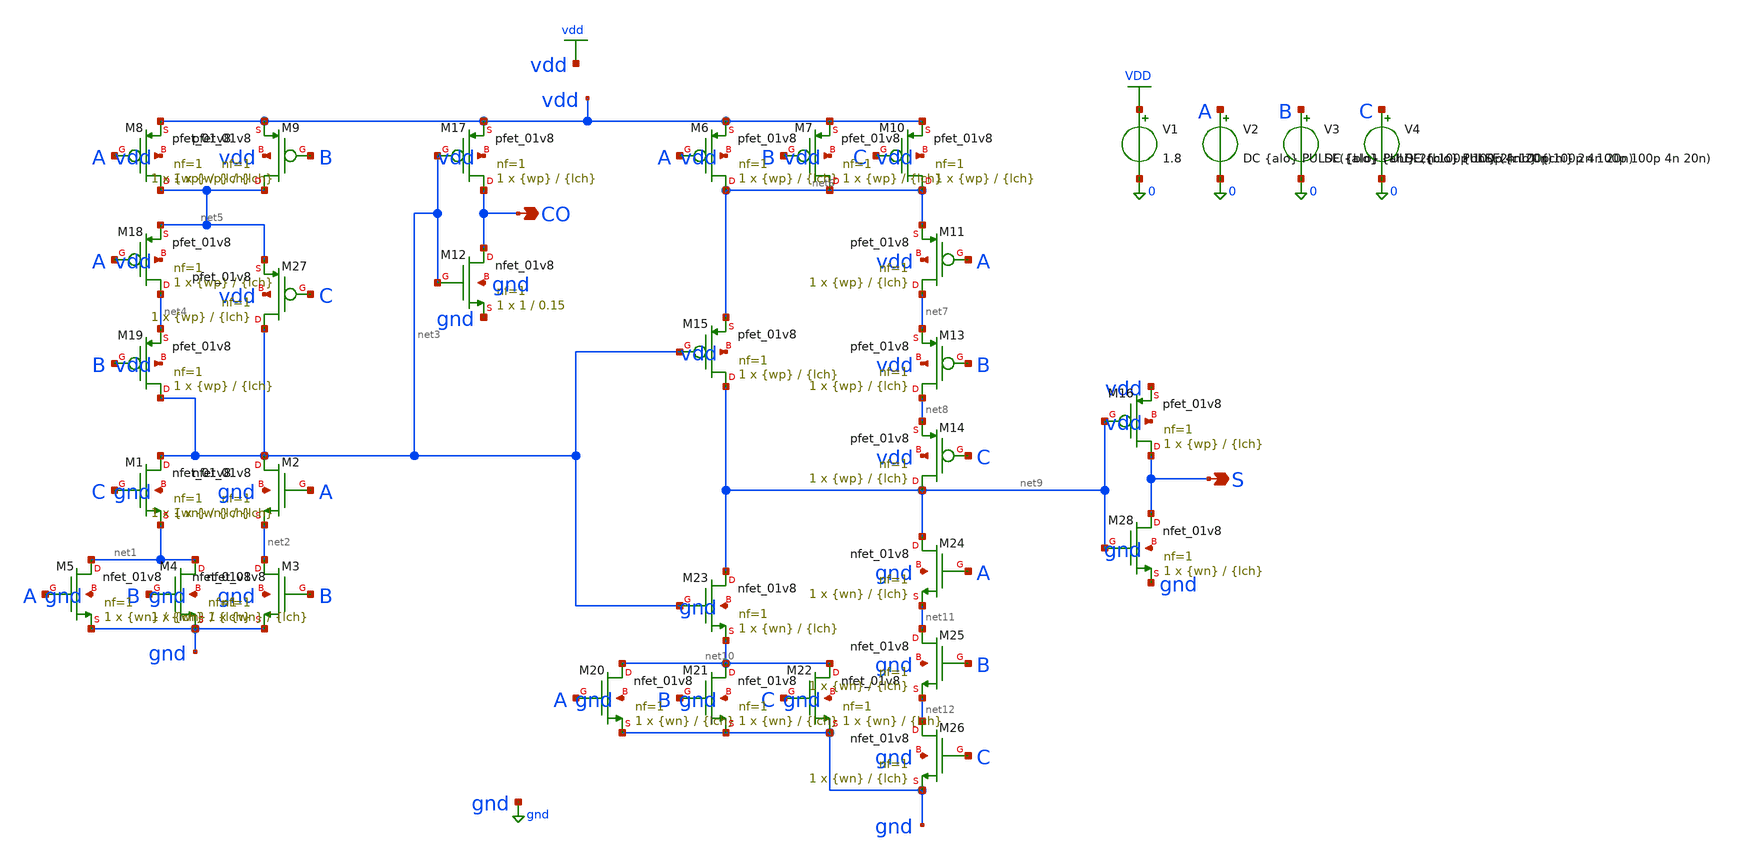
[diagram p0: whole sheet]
** sch_path: tb_delay.sch
**.subckt tb_delay CO S
*.opin CO
*.opin S
XM2 net3 A net2 gnd sky130_fd_pr__nfet_01v8 L={lch} W={wn} nf=1 ad='int((1 + 1)/2) * {wn} / 1 * 0.29'
+ as='int((1 + 2)/2) * {wn} / 1 * 0.29' pd='2*int((1 + 1)/2) * ({wn} / 1 + 0.29)' ps='2*int((1 + 2)/2) * ({wn} / 1 + 0.29)'
+ nrd='0.29 / {wn} ' nrs='0.29 / {wn} ' sa=0 sb=0 sd=0 mult=1 m=1
XM8 net5 A vdd vdd sky130_fd_pr__pfet_01v8 L={lch} W={wp} nf=1 ad='int((1 + 1)/2) * {wp} / 1 * 0.29'
+ as='int((1 + 2)/2) * {wp} / 1 * 0.29' pd='2*int((1 + 1)/2) * ({wp} / 1 + 0.29)' ps='2*int((1 + 2)/2) * ({wp} / 1 + 0.29)'
+ nrd='0.29 / {wp} ' nrs='0.29 / {wp} ' sa=0 sb=0 sd=0 mult=1 m=1
XM12 CO net3 gnd gnd sky130_fd_pr__nfet_01v8 L=0.15 W=1 nf=1 ad='int((1 + 1)/2) * 1 / 1 * 0.29' as='int((1 + 2)/2) * 1 / 1 * 0.29'
+ pd='2*int((1 + 1)/2) * (1 / 1 + 0.29)' ps='2*int((1 + 2)/2) * (1 / 1 + 0.29)' nrd='0.29 / 1 ' nrs='0.29 / 1 '
+ sa=0 sb=0 sd=0 mult=1 m=1
V1 VDD 0 1.8
V2 A 0 DC {alo} PULSE({alo} {ahi} 2n 100p 100p 4n 20n)
V3 B 0 DC {blo} PULSE({blo} {bhi} 2n 100p 100p 4n 20n)
V4 C 0 DC {clo} PULSE({clo} {chi} 2n 100p 100p 4n 20n)
XM9 net5 B vdd vdd sky130_fd_pr__pfet_01v8 L={lch} W={wp} nf=1 ad='int((1 + 1)/2) * {wp} / 1 * 0.29'
+ as='int((1 + 2)/2) * {wp} / 1 * 0.29' pd='2*int((1 + 1)/2) * ({wp} / 1 + 0.29)' ps='2*int((1 + 2)/2) * ({wp} / 1 + 0.29)'
+ nrd='0.29 / {wp} ' nrs='0.29 / {wp} ' sa=0 sb=0 sd=0 mult=1 m=1
XM6 net6 A vdd vdd sky130_fd_pr__pfet_01v8 L={lch} W={wp} nf=1 ad='int((1 + 1)/2) * {wp} / 1 * 0.29'
+ as='int((1 + 2)/2) * {wp} / 1 * 0.29' pd='2*int((1 + 1)/2) * ({wp} / 1 + 0.29)' ps='2*int((1 + 2)/2) * ({wp} / 1 + 0.29)'
+ nrd='0.29 / {wp} ' nrs='0.29 / {wp} ' sa=0 sb=0 sd=0 mult=1 m=1
XM7 net6 B vdd vdd sky130_fd_pr__pfet_01v8 L={lch} W={wp} nf=1 ad='int((1 + 1)/2) * {wp} / 1 * 0.29'
+ as='int((1 + 2)/2) * {wp} / 1 * 0.29' pd='2*int((1 + 1)/2) * ({wp} / 1 + 0.29)' ps='2*int((1 + 2)/2) * ({wp} / 1 + 0.29)'
+ nrd='0.29 / {wp} ' nrs='0.29 / {wp} ' sa=0 sb=0 sd=0 mult=1 m=1
XM10 net6 C vdd vdd sky130_fd_pr__pfet_01v8 L={lch} W={wp} nf=1 ad='int((1 + 1)/2) * {wp} / 1 * 0.29'
+ as='int((1 + 2)/2) * {wp} / 1 * 0.29' pd='2*int((1 + 1)/2) * ({wp} / 1 + 0.29)' ps='2*int((1 + 2)/2) * ({wp} / 1 + 0.29)'
+ nrd='0.29 / {wp} ' nrs='0.29 / {wp} ' sa=0 sb=0 sd=0 mult=1 m=1
XM11 net7 A net6 vdd sky130_fd_pr__pfet_01v8 L={lch} W={wp} nf=1 ad='int((1 + 1)/2) * {wp} / 1 * 0.29'
+ as='int((1 + 2)/2) * {wp} / 1 * 0.29' pd='2*int((1 + 1)/2) * ({wp} / 1 + 0.29)' ps='2*int((1 + 2)/2) * ({wp} / 1 + 0.29)'
+ nrd='0.29 / {wp} ' nrs='0.29 / {wp} ' sa=0 sb=0 sd=0 mult=1 m=1
XM13 net8 B net7 vdd sky130_fd_pr__pfet_01v8 L={lch} W={wp} nf=1 ad='int((1 + 1)/2) * {wp} / 1 * 0.29'
+ as='int((1 + 2)/2) * {wp} / 1 * 0.29' pd='2*int((1 + 1)/2) * ({wp} / 1 + 0.29)' ps='2*int((1 + 2)/2) * ({wp} / 1 + 0.29)'
+ nrd='0.29 / {wp} ' nrs='0.29 / {wp} ' sa=0 sb=0 sd=0 mult=1 m=1
XM14 net9 C net8 vdd sky130_fd_pr__pfet_01v8 L={lch} W={wp} nf=1 ad='int((1 + 1)/2) * {wp} / 1 * 0.29'
+ as='int((1 + 2)/2) * {wp} / 1 * 0.29' pd='2*int((1 + 1)/2) * ({wp} / 1 + 0.29)' ps='2*int((1 + 2)/2) * ({wp} / 1 + 0.29)'
+ nrd='0.29 / {wp} ' nrs='0.29 / {wp} ' sa=0 sb=0 sd=0 mult=1 m=1
XM15 net9 net3 net6 vdd sky130_fd_pr__pfet_01v8 L={lch} W={wp} nf=1 ad='int((1 + 1)/2) * {wp} / 1 * 0.29'
+ as='int((1 + 2)/2) * {wp} / 1 * 0.29' pd='2*int((1 + 1)/2) * ({wp} / 1 + 0.29)' ps='2*int((1 + 2)/2) * ({wp} / 1 + 0.29)'
+ nrd='0.29 / {wp} ' nrs='0.29 / {wp} ' sa=0 sb=0 sd=0 mult=1 m=1
XM16 S net9 vdd vdd sky130_fd_pr__pfet_01v8 L={lch} W={wp} nf=1 ad='int((1 + 1)/2) * {wp} / 1 * 0.29'
+ as='int((1 + 2)/2) * {wp} / 1 * 0.29' pd='2*int((1 + 1)/2) * ({wp} / 1 + 0.29)' ps='2*int((1 + 2)/2) * ({wp} / 1 + 0.29)'
+ nrd='0.29 / {wp} ' nrs='0.29 / {wp} ' sa=0 sb=0 sd=0 mult=1 m=1
XM17 CO net3 vdd vdd sky130_fd_pr__pfet_01v8 L={lch} W={wp} nf=1 ad='int((1 + 1)/2) * {wp} / 1 * 0.29'
+ as='int((1 + 2)/2) * {wp} / 1 * 0.29' pd='2*int((1 + 1)/2) * ({wp} / 1 + 0.29)' ps='2*int((1 + 2)/2) * ({wp} / 1 + 0.29)'
+ nrd='0.29 / {wp} ' nrs='0.29 / {wp} ' sa=0 sb=0 sd=0 mult=1 m=1
XM18 net4 A net5 vdd sky130_fd_pr__pfet_01v8 L={lch} W={wp} nf=1 ad='int((1 + 1)/2) * {wp} / 1 * 0.29'
+ as='int((1 + 2)/2) * {wp} / 1 * 0.29' pd='2*int((1 + 1)/2) * ({wp} / 1 + 0.29)' ps='2*int((1 + 2)/2) * ({wp} / 1 + 0.29)'
+ nrd='0.29 / {wp} ' nrs='0.29 / {wp} ' sa=0 sb=0 sd=0 mult=1 m=1
XM19 net3 B net4 vdd sky130_fd_pr__pfet_01v8 L={lch} W={wp} nf=1 ad='int((1 + 1)/2) * {wp} / 1 * 0.29'
+ as='int((1 + 2)/2) * {wp} / 1 * 0.29' pd='2*int((1 + 1)/2) * ({wp} / 1 + 0.29)' ps='2*int((1 + 2)/2) * ({wp} / 1 + 0.29)'
+ nrd='0.29 / {wp} ' nrs='0.29 / {wp} ' sa=0 sb=0 sd=0 mult=1 m=1
XM27 net3 C net5 vdd sky130_fd_pr__pfet_01v8 L={lch} W={wp} nf=1 ad='int((1 + 1)/2) * {wp} / 1 * 0.29'
+ as='int((1 + 2)/2) * {wp} / 1 * 0.29' pd='2*int((1 + 1)/2) * ({wp} / 1 + 0.29)' ps='2*int((1 + 2)/2) * ({wp} / 1 + 0.29)'
+ nrd='0.29 / {wp} ' nrs='0.29 / {wp} ' sa=0 sb=0 sd=0 mult=1 m=1
XM1 net3 C net1 gnd sky130_fd_pr__nfet_01v8 L={lch} W={wn} nf=1 ad='int((1 + 1)/2) * {wn} / 1 * 0.29'
+ as='int((1 + 2)/2) * {wn} / 1 * 0.29' pd='2*int((1 + 1)/2) * ({wn} / 1 + 0.29)' ps='2*int((1 + 2)/2) * ({wn} / 1 + 0.29)'
+ nrd='0.29 / {wn} ' nrs='0.29 / {wn} ' sa=0 sb=0 sd=0 mult=1 m=1
XM3 net2 B gnd gnd sky130_fd_pr__nfet_01v8 L={lch} W={wn} nf=1 ad='int((1 + 1)/2) * {wn} / 1 * 0.29'
+ as='int((1 + 2)/2) * {wn} / 1 * 0.29' pd='2*int((1 + 1)/2) * ({wn} / 1 + 0.29)' ps='2*int((1 + 2)/2) * ({wn} / 1 + 0.29)'
+ nrd='0.29 / {wn} ' nrs='0.29 / {wn} ' sa=0 sb=0 sd=0 mult=1 m=1
XM4 net1 B gnd gnd sky130_fd_pr__nfet_01v8 L={lch} W={wn} nf=1 ad='int((1 + 1)/2) * {wn} / 1 * 0.29'
+ as='int((1 + 2)/2) * {wn} / 1 * 0.29' pd='2*int((1 + 1)/2) * ({wn} / 1 + 0.29)' ps='2*int((1 + 2)/2) * ({wn} / 1 + 0.29)'
+ nrd='0.29 / {wn} ' nrs='0.29 / {wn} ' sa=0 sb=0 sd=0 mult=1 m=1
XM5 net1 A gnd gnd sky130_fd_pr__nfet_01v8 L={lch} W={wn} nf=1 ad='int((1 + 1)/2) * {wn} / 1 * 0.29'
+ as='int((1 + 2)/2) * {wn} / 1 * 0.29' pd='2*int((1 + 1)/2) * ({wn} / 1 + 0.29)' ps='2*int((1 + 2)/2) * ({wn} / 1 + 0.29)'
+ nrd='0.29 / {wn} ' nrs='0.29 / {wn} ' sa=0 sb=0 sd=0 mult=1 m=1
XM20 net10 A gnd gnd sky130_fd_pr__nfet_01v8 L={lch} W={wn} nf=1 ad='int((1 + 1)/2) * {wn} / 1 * 0.29'
+ as='int((1 + 2)/2) * {wn} / 1 * 0.29' pd='2*int((1 + 1)/2) * ({wn} / 1 + 0.29)' ps='2*int((1 + 2)/2) * ({wn} / 1 + 0.29)'
+ nrd='0.29 / {wn} ' nrs='0.29 / {wn} ' sa=0 sb=0 sd=0 mult=1 m=1
XM21 net10 B gnd gnd sky130_fd_pr__nfet_01v8 L={lch} W={wn} nf=1 ad='int((1 + 1)/2) * {wn} / 1 * 0.29'
+ as='int((1 + 2)/2) * {wn} / 1 * 0.29' pd='2*int((1 + 1)/2) * ({wn} / 1 + 0.29)' ps='2*int((1 + 2)/2) * ({wn} / 1 + 0.29)'
+ nrd='0.29 / {wn} ' nrs='0.29 / {wn} ' sa=0 sb=0 sd=0 mult=1 m=1
XM22 net10 C gnd gnd sky130_fd_pr__nfet_01v8 L={lch} W={wn} nf=1 ad='int((1 + 1)/2) * {wn} / 1 * 0.29'
+ as='int((1 + 2)/2) * {wn} / 1 * 0.29' pd='2*int((1 + 1)/2) * ({wn} / 1 + 0.29)' ps='2*int((1 + 2)/2) * ({wn} / 1 + 0.29)'
+ nrd='0.29 / {wn} ' nrs='0.29 / {wn} ' sa=0 sb=0 sd=0 mult=1 m=1
XM23 net9 net3 net10 gnd sky130_fd_pr__nfet_01v8 L={lch} W={wn} nf=1 ad='int((1 + 1)/2) * {wn} / 1 * 0.29'
+ as='int((1 + 2)/2) * {wn} / 1 * 0.29' pd='2*int((1 + 1)/2) * ({wn} / 1 + 0.29)' ps='2*int((1 + 2)/2) * ({wn} / 1 + 0.29)'
+ nrd='0.29 / {wn} ' nrs='0.29 / {wn} ' sa=0 sb=0 sd=0 mult=1 m=1
XM24 net9 A net11 gnd sky130_fd_pr__nfet_01v8 L={lch} W={wn} nf=1 ad='int((1 + 1)/2) * {wn} / 1 * 0.29'
+ as='int((1 + 2)/2) * {wn} / 1 * 0.29' pd='2*int((1 + 1)/2) * ({wn} / 1 + 0.29)' ps='2*int((1 + 2)/2) * ({wn} / 1 + 0.29)'
+ nrd='0.29 / {wn} ' nrs='0.29 / {wn} ' sa=0 sb=0 sd=0 mult=1 m=1
XM25 net11 B net12 gnd sky130_fd_pr__nfet_01v8 L={lch} W={wn} nf=1 ad='int((1 + 1)/2) * {wn} / 1 * 0.29'
+ as='int((1 + 2)/2) * {wn} / 1 * 0.29' pd='2*int((1 + 1)/2) * ({wn} / 1 + 0.29)' ps='2*int((1 + 2)/2) * ({wn} / 1 + 0.29)'
+ nrd='0.29 / {wn} ' nrs='0.29 / {wn} ' sa=0 sb=0 sd=0 mult=1 m=1
XM26 net12 C gnd gnd sky130_fd_pr__nfet_01v8 L={lch} W={wn} nf=1 ad='int((1 + 1)/2) * {wn} / 1 * 0.29'
+ as='int((1 + 2)/2) * {wn} / 1 * 0.29' pd='2*int((1 + 1)/2) * ({wn} / 1 + 0.29)' ps='2*int((1 + 2)/2) * ({wn} / 1 + 0.29)'
+ nrd='0.29 / {wn} ' nrs='0.29 / {wn} ' sa=0 sb=0 sd=0 mult=1 m=1
XM28 S net9 gnd gnd sky130_fd_pr__nfet_01v8 L={lch} W={wn} nf=1 ad='int((1 + 1)/2) * {wn} / 1 * 0.29'
+ as='int((1 + 2)/2) * {wn} / 1 * 0.29' pd='2*int((1 + 1)/2) * ({wn} / 1 + 0.29)' ps='2*int((1 + 2)/2) * ({wn} / 1 + 0.29)'
+ nrd='0.29 / {wn} ' nrs='0.29 / {wn} ' sa=0 sb=0 sd=0 mult=1 m=1
**** begin user architecture code

.lib /foss/pdks/sky130A/libs.tech/ngspice/sky130.lib.spice tt

.param wp=2.5 wn=1 lch=0.15
.param alo=0 ahi=1.8 blo=0 bhi=0 clo=0 chi=0

.control
echo Ratio SUM_AVG_ps SUM_WORST_ps COUT_AVG_ps COUT_WORST_ps ALL_AVG_ps ALL_WORST_ps >
+ /foss/designs/tpd_fulladder.txt

foreach w 2.5 2.6 2.7 2.8 2.9 3.0
    setplot const
    let sum_s = 0
    let sum_co = 0
    let worst_s = 0
    let worst_co = 0

    alterparam wp = $w

    foreach sel 1 2 3
        foreach u 0 1.8
            foreach v 0 1.8

                if $sel = 1
                    set pin = a
                    alterparam alo = 0
                    alterparam ahi = 1.8
                    alterparam blo = $u
                    alterparam bhi = $u
                    alterparam clo = $v
                    alterparam chi = $v
                end

                if $sel = 2
                    set pin = b
                    alterparam alo = $u
                    alterparam ahi = $u
                    alterparam blo = 0
                    alterparam bhi = 1.8
                    alterparam clo = $v
                    alterparam chi = $v
                end

                if $sel = 3
                    set pin = c
                    alterparam alo = $u
                    alterparam ahi = $u
                    alterparam blo = $v
                    alterparam bhi = $v
                    alterparam clo = 0
                    alterparam chi = 1.8
                end

                reset
                tran 5p 10n

                if $u = $v
                    meas tran slh TRIG v($pin) VAL=0.9 RISE=1 TD=1.9n TARG v(s) VAL=0.9 RISE=1
+ TD=1.9n
                    meas tran shl TRIG v($pin) VAL=0.9 FALL=1 TD=6n TARG v(s) VAL=0.9 FALL=1 TD=6n
                else
                    meas tran shl TRIG v($pin) VAL=0.9 RISE=1 TD=1.9n TARG v(s) VAL=0.9 FALL=1
+ TD=1.9n
                    meas tran slh TRIG v($pin) VAL=0.9 FALL=1 TD=6n TARG v(s) VAL=0.9 RISE=1 TD=6n

                    meas tran clh TRIG v($pin) VAL=0.9 RISE=1 TD=1.9n TARG v(co) VAL=0.9 RISE=1
+ TD=1.9n
                    meas tran chl TRIG v($pin) VAL=0.9 FALL=1 TD=6n TARG v(co) VAL=0.9 FALL=1 TD=6n
                end

                set ds_lh = "$&slh"
                set ds_hl = "$&shl"

                if $u <> $v
                    set dc_lh = "$&clh"
                    set dc_hl = "$&chl"
                end

                setplot const

                let sum_s = sum_s + $ds_lh + $ds_hl
                let worst_s = (worst_s + $ds_lh + abs(worst_s-$ds_lh))/2
                let worst_s = (worst_s + $ds_hl + abs(worst_s-$ds_hl))/2

                if $u <> $v
                    let sum_co = sum_co + $dc_lh + $dc_hl
                    let worst_co = (worst_co + $dc_lh + abs(worst_co-$dc_lh))/2
                    let worst_co = (worst_co + $dc_hl + abs(worst_co-$dc_hl))/2
                end

            end
        end
    end

    let avg_s = sum_s*1e12/24
    let avg_co = sum_co*1e12/12
    let avg_all = (sum_s+sum_co)*1e12/36

    let ws_ps = worst_s*1e12
    let wc_ps = worst_co*1e12
    let worst_all = (worst_s+worst_co+abs(worst_s-worst_co))*1e12/2

    echo $w $&avg_s $&ws_ps $&avg_co $&wc_ps $&avg_all $&worst_all >>
+ /foss/designs/tpd_fulladder.txt

end
.endc

.end




**** end user architecture code
**.ends
.GLOBAL vdd
.GLOBAL gnd
.GLOBAL VDD
.end
